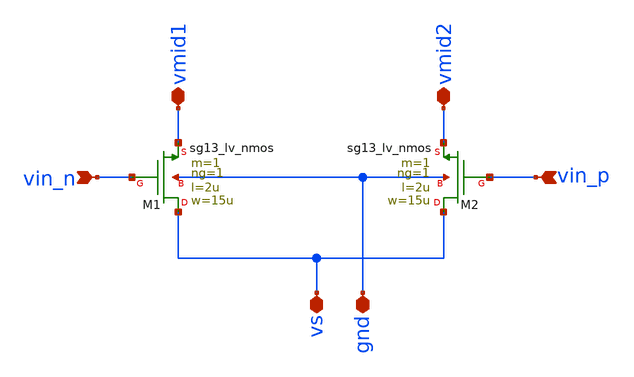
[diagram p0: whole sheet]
** sch_path: AC3E-IHP_ALDO/design_data/klayout/lvs/diff_pair/nmos_diffpar.sch
**.subckt nmos_diffpar vin_n vin_p vmid1 vmid2 vs gnd
*.ipin vin_n
*.ipin vin_p
*.iopin vmid1
*.iopin vmid2
*.iopin vs
*.iopin gnd
XM1 vs vin_n vmid1 gnd sg13_lv_nmos w=15u l=2u ng=1 m=1 mm_ok=1
XM2 vs vin_p vmid2 gnd sg13_lv_nmos w=15u l=2u ng=1 m=1 mm_ok=1
**.ends
.end
